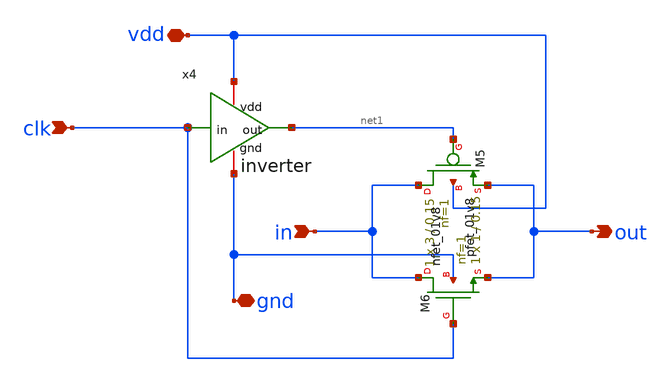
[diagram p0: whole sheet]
** sch_path: transmission_gate.sch
**.subckt transmission_gate in out gnd vdd clk
*.ipin in
*.opin out
*.iopin gnd
*.iopin vdd
*.ipin clk
x4 vdd clk net1 gnd inverter
XM5 in net1 out vdd sky130_fd_pr__pfet_01v8 L=0.15 W=3 nf=1 ad='int((nf+1)/2) * W/nf * 0.29' as='int((nf+2)/2) * W/nf * 0.29'
+ pd='2*int((nf+1)/2) * (W/nf + 0.29)' ps='2*int((nf+2)/2) * (W/nf + 0.29)' nrd='0.29 / W' nrs='0.29 / W'
+ sa=0 sb=0 sd=0 mult=1 m=1
XM6 in clk out gnd sky130_fd_pr__nfet_01v8 L=0.15 W=1 nf=1 ad='int((1 + 1)/2) * 1 / 1 * 0.29' as='int((1 + 2)/2) * 1 / 1 * 0.29'
+ pd='2*int((1 + 1)/2) * (1 / 1 + 0.29)' ps='2*int((1 + 2)/2) * (1 / 1 + 0.29)' nrd='0.29 / 1 ' nrs='0.29 / 1 '
+ sa=0 sb=0 sd=0 mult=1 m=1
**.ends

* expanding   symbol:  /foss/designs/sar_adc/inverter.sym # of pins=4
** sym_path: inverter.sym
** sch_path: inverter.sch
.subckt inverter vdd in out gnd
*.iopin vdd
*.iopin gnd
*.ipin in
*.opin out
XM2 out in gnd gnd sky130_fd_pr__nfet_01v8 L=0.15 W=1 nf=1 ad='int((1 + 1)/2) * 1 / 1 * 0.29' as='int((1 + 2)/2) * 1 / 1 * 0.29'
+ pd='2*int((1 + 1)/2) * (1 / 1 + 0.29)' ps='2*int((1 + 2)/2) * (1 / 1 + 0.29)' nrd='0.29 / 1 ' nrs='0.29 / 1 '
+ sa=0 sb=0 sd=0 mult=1 m=1
XM11 out in vdd vdd sky130_fd_pr__pfet_01v8 L=0.15 W=3 nf=1 ad='int((nf+1)/2) * W/nf * 0.29' as='int((nf+2)/2) * W/nf * 0.29'
+ pd='2*int((nf+1)/2) * (W/nf + 0.29)' ps='2*int((nf+2)/2) * (W/nf + 0.29)' nrd='0.29 / W' nrs='0.29 / W'
+ sa=0 sb=0 sd=0 mult=1 m=1
.ends

.end
